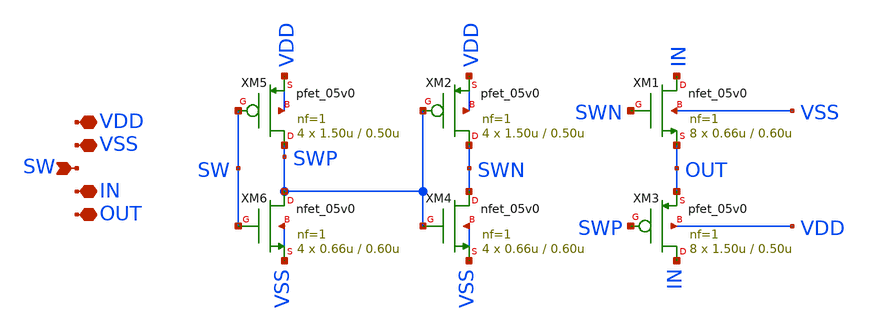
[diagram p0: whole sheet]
** sch_path: xschem/switch-matrix/transmission_gate.sch
**.subckt transmission_gate VDD VSS IN OUT SW
*.iopin VDD
*.iopin VSS
*.iopin IN
*.iopin OUT
*.ipin SW
XM3 IN SWP OUT VDD pfet_05v0 L=0.50u W=1.50u nf=1 ad='int((nf+1)/2) * W/nf * 0.18u' as='int((nf+2)/2) * W/nf * 0.18u'
+ pd='2*int((nf+1)/2) * (W/nf + 0.18u)' ps='2*int((nf+2)/2) * (W/nf + 0.18u)' nrd='0.18u / W' nrs='0.18u / W'
+ sa=0 sb=0 sd=0 m=8
XM1 IN SWN OUT VSS nfet_05v0 L=0.60u W=0.66u nf=1 ad='int((nf+1)/2) * W/nf * 0.18u' as='int((nf+2)/2) * W/nf * 0.18u'
+ pd='2*int((nf+1)/2) * (W/nf + 0.18u)' ps='2*int((nf+2)/2) * (W/nf + 0.18u)' nrd='0.18u / W' nrs='0.18u / W'
+ sa=0 sb=0 sd=0 m=8
XM2 SWN SWP VDD VDD pfet_05v0 L=0.50u W=1.50u nf=1 ad='int((nf+1)/2) * W/nf * 0.18u' as='int((nf+2)/2) * W/nf * 0.18u'
+ pd='2*int((nf+1)/2) * (W/nf + 0.18u)' ps='2*int((nf+2)/2) * (W/nf + 0.18u)' nrd='0.18u / W' nrs='0.18u / W'
+ sa=0 sb=0 sd=0 m=4
XM4 SWN SWP VSS VSS nfet_05v0 L=0.60u W=0.66u nf=1 ad='int((nf+1)/2) * W/nf * 0.18u' as='int((nf+2)/2) * W/nf * 0.18u'
+ pd='2*int((nf+1)/2) * (W/nf + 0.18u)' ps='2*int((nf+2)/2) * (W/nf + 0.18u)' nrd='0.18u / W' nrs='0.18u / W'
+ sa=0 sb=0 sd=0 m=4
XM5 SWP SW VDD VDD pfet_05v0 L=0.50u W=1.50u nf=1 ad='int((nf+1)/2) * W/nf * 0.18u' as='int((nf+2)/2) * W/nf * 0.18u'
+ pd='2*int((nf+1)/2) * (W/nf + 0.18u)' ps='2*int((nf+2)/2) * (W/nf + 0.18u)' nrd='0.18u / W' nrs='0.18u / W'
+ sa=0 sb=0 sd=0 m=4
XM6 SWP SW VSS VSS nfet_05v0 L=0.60u W=0.66u nf=1 ad='int((nf+1)/2) * W/nf * 0.18u' as='int((nf+2)/2) * W/nf * 0.18u'
+ pd='2*int((nf+1)/2) * (W/nf + 0.18u)' ps='2*int((nf+2)/2) * (W/nf + 0.18u)' nrd='0.18u / W' nrs='0.18u / W'
+ sa=0 sb=0 sd=0 m=4
**.ends
.end
